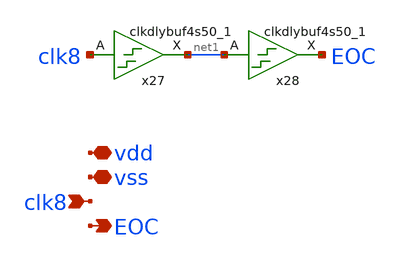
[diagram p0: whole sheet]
** sch_path: xschem/sar-adc/EOC_delay.sch
**.subckt EOC_delay clk8 vdd vss EOC
*.ipin clk8
*.iopin vdd
*.iopin vss
*.opin EOC
x27 clk8 vss vss vdd vdd net1 sky130_fd_sc_hd__clkdlybuf4s50_1
x28 net1 vss vss vdd vdd EOC sky130_fd_sc_hd__clkdlybuf4s50_1
**.ends
.end
